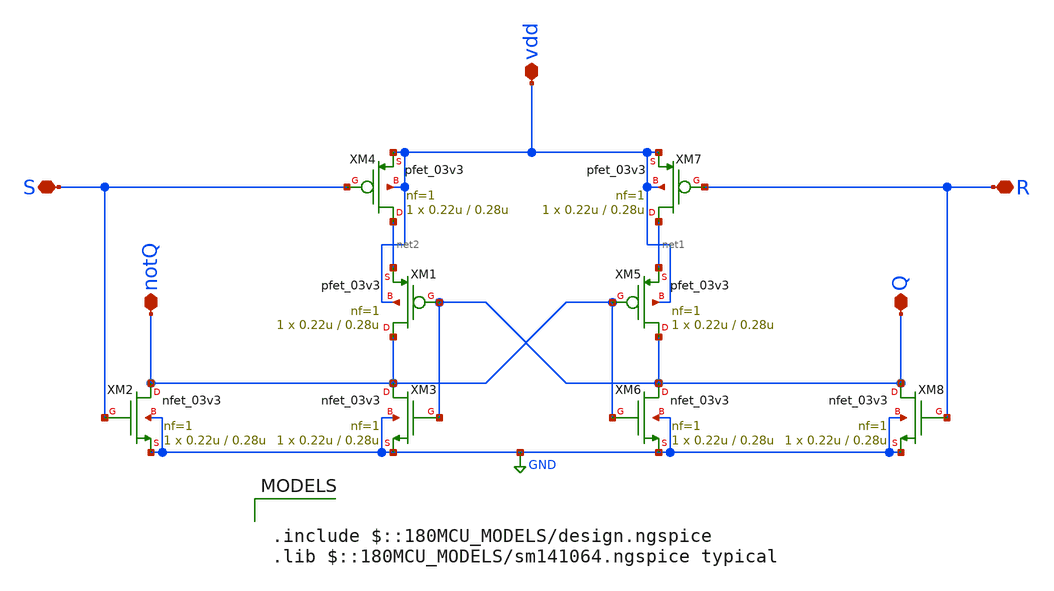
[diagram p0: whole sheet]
** sch_path: Clock_Reference/clockGenerator/clockGenerator/clockGenerator/RS.sch
**.subckt RS R S vdd notQ Q
*.iopin R
*.iopin S
*.iopin vdd
*.iopin notQ
*.iopin Q
XM1 notQ Q net2 vdd pfet_03v3 L=0.28u W=0.22u nf=1 ad='int((nf+1)/2) * W/nf * 0.18u' as='int((nf+2)/2) * W/nf * 0.18u'
+ pd='2*int((nf+1)/2) * (W/nf + 0.18u)' ps='2*int((nf+2)/2) * (W/nf + 0.18u)' nrd='0.18u / W' nrs='0.18u / W'
+ sa=0 sb=0 sd=0 m=1
XM2 notQ S GND GND nfet_03v3 L=0.28u W=0.22u nf=1 ad='int((nf+1)/2) * W/nf * 0.18u' as='int((nf+2)/2) * W/nf * 0.18u'
+ pd='2*int((nf+1)/2) * (W/nf + 0.18u)' ps='2*int((nf+2)/2) * (W/nf + 0.18u)' nrd='0.18u / W' nrs='0.18u / W'
+ sa=0 sb=0 sd=0 m=1
XM3 notQ Q GND GND nfet_03v3 L=0.28u W=0.22u nf=1 ad='int((nf+1)/2) * W/nf * 0.18u' as='int((nf+2)/2) * W/nf * 0.18u'
+ pd='2*int((nf+1)/2) * (W/nf + 0.18u)' ps='2*int((nf+2)/2) * (W/nf + 0.18u)' nrd='0.18u / W' nrs='0.18u / W'
+ sa=0 sb=0 sd=0 m=1
XM4 net2 S vdd vdd pfet_03v3 L=0.28u W=0.22u nf=1 ad='int((nf+1)/2) * W/nf * 0.18u' as='int((nf+2)/2) * W/nf * 0.18u'
+ pd='2*int((nf+1)/2) * (W/nf + 0.18u)' ps='2*int((nf+2)/2) * (W/nf + 0.18u)' nrd='0.18u / W' nrs='0.18u / W'
+ sa=0 sb=0 sd=0 m=1
XM5 Q notQ net1 vdd pfet_03v3 L=0.28u W=0.22u nf=1 ad='int((nf+1)/2) * W/nf * 0.18u' as='int((nf+2)/2) * W/nf * 0.18u'
+ pd='2*int((nf+1)/2) * (W/nf + 0.18u)' ps='2*int((nf+2)/2) * (W/nf + 0.18u)' nrd='0.18u / W' nrs='0.18u / W'
+ sa=0 sb=0 sd=0 m=1
XM6 Q notQ GND GND nfet_03v3 L=0.28u W=0.22u nf=1 ad='int((nf+1)/2) * W/nf * 0.18u' as='int((nf+2)/2) * W/nf * 0.18u'
+ pd='2*int((nf+1)/2) * (W/nf + 0.18u)' ps='2*int((nf+2)/2) * (W/nf + 0.18u)' nrd='0.18u / W' nrs='0.18u / W'
+ sa=0 sb=0 sd=0 m=1
XM7 net1 R vdd vdd pfet_03v3 L=0.28u W=0.22u nf=1 ad='int((nf+1)/2) * W/nf * 0.18u' as='int((nf+2)/2) * W/nf * 0.18u'
+ pd='2*int((nf+1)/2) * (W/nf + 0.18u)' ps='2*int((nf+2)/2) * (W/nf + 0.18u)' nrd='0.18u / W' nrs='0.18u / W'
+ sa=0 sb=0 sd=0 m=1
XM8 Q R GND GND nfet_03v3 L=0.28u W=0.22u nf=1 ad='int((nf+1)/2) * W/nf * 0.18u' as='int((nf+2)/2) * W/nf * 0.18u'
+ pd='2*int((nf+1)/2) * (W/nf + 0.18u)' ps='2*int((nf+2)/2) * (W/nf + 0.18u)' nrd='0.18u / W' nrs='0.18u / W'
+ sa=0 sb=0 sd=0 m=1
**** begin user architecture code

.include $::180MCU_MODELS/design.ngspice
.lib $::180MCU_MODELS/sm141064.ngspice typical

**** end user architecture code
**.ends
.GLOBAL GND
.end
